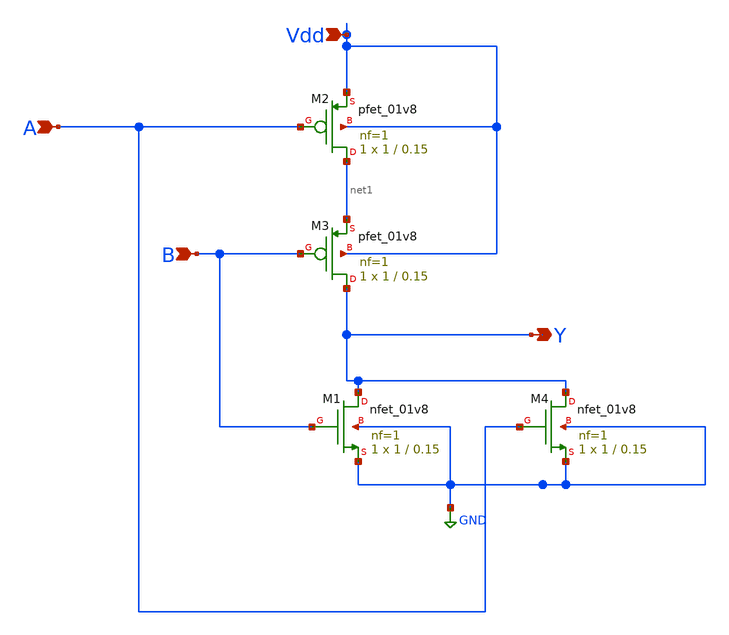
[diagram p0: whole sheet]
** sch_path: Blocks/main_comparator/OR_gate/a1.sch
**.subckt a1 A B Y Vdd
*.ipin A
*.ipin B
*.opin Y
*.ipin Vdd
XM1 Y B GND GND sky130_fd_pr__nfet_01v8 L=0.15 W=1 nf=1 ad='int((nf+1)/2) * W/nf * 0.29' as='int((nf+2)/2) * W/nf * 0.29'
+ pd='2*int((nf+1)/2) * (W/nf + 0.29)' ps='2*int((nf+2)/2) * (W/nf + 0.29)' nrd='0.29 / W' nrs='0.29 / W'
+ sa=0 sb=0 sd=0 mult=1 m=1
XM2 net1 A Vdd Vdd sky130_fd_pr__pfet_01v8 L=0.15 W=1 nf=1 ad='int((nf+1)/2) * W/nf * 0.29' as='int((nf+2)/2) * W/nf * 0.29'
+ pd='2*int((nf+1)/2) * (W/nf + 0.29)' ps='2*int((nf+2)/2) * (W/nf + 0.29)' nrd='0.29 / W' nrs='0.29 / W'
+ sa=0 sb=0 sd=0 mult=1 m=1
XM3 Y B net1 Vdd sky130_fd_pr__pfet_01v8 L=0.15 W=1 nf=1 ad='int((nf+1)/2) * W/nf * 0.29' as='int((nf+2)/2) * W/nf * 0.29'
+ pd='2*int((nf+1)/2) * (W/nf + 0.29)' ps='2*int((nf+2)/2) * (W/nf + 0.29)' nrd='0.29 / W' nrs='0.29 / W'
+ sa=0 sb=0 sd=0 mult=1 m=1
XM4 Y A GND GND sky130_fd_pr__nfet_01v8 L=0.15 W=1 nf=1 ad='int((nf+1)/2) * W/nf * 0.29' as='int((nf+2)/2) * W/nf * 0.29'
+ pd='2*int((nf+1)/2) * (W/nf + 0.29)' ps='2*int((nf+2)/2) * (W/nf + 0.29)' nrd='0.29 / W' nrs='0.29 / W'
+ sa=0 sb=0 sd=0 mult=1 m=1
**.ends
.GLOBAL GND
.end
